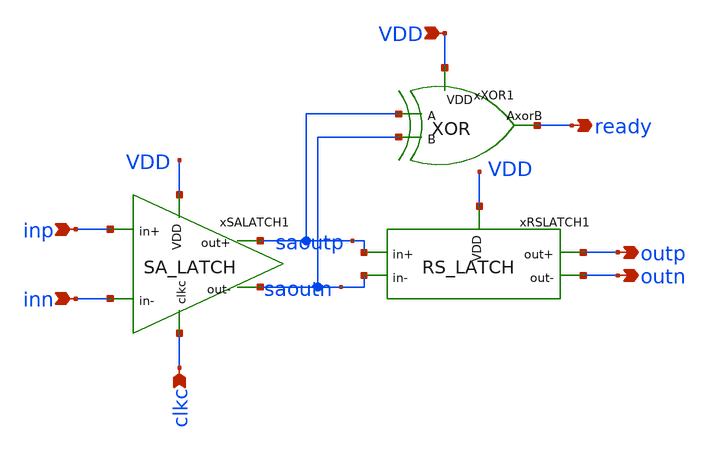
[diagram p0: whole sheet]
** sch_path: Design_Files/IC Design/Schematic/SAR_ADC_BLOCKS/COMP/COMP.sch
**.subckt COMP VDD inp inn outp outn clkc ready
*.ipin VDD
*.ipin inp
*.ipin inn
*.opin outp
*.opin outn
*.ipin clkc
*.opin ready
xXOR1 VDD ready saoutp saoutn XOR
xRSLATCH1 VDD outp outn saoutp saoutn RS_LATCH
xSALATCH1 VDD clkc saoutp saoutn inn inp SA_LATCH
**.ends

* expanding   symbol:  ECG_Acquisition_IC/Design_Files/IC
*+ Design/Schematic/SAR_ADC_BLOCKS/XOR/XOR.sym # of pins=4
** sym_path: Design_Files/IC Design/Schematic/SAR_ADC_BLOCKS/XOR/XOR.sym
** sch_path: Design_Files/IC Design/Schematic/SAR_ADC_BLOCKS/XOR/XOR.sch
.subckt XOR VDD AxorB A B
*.ipin VDD
*.ipin A
*.ipin B
*.opin AxorB
XM1 Abar A 0 0 nfet_03v3 L=0.28u W=0.5u nf=1 ad='int((nf+1)/2) * W/nf * 0.18u' as='int((nf+2)/2) * W/nf * 0.18u'
+ pd='2*int((nf+1)/2) * (W/nf + 0.18u)' ps='2*int((nf+2)/2) * (W/nf + 0.18u)' nrd='0.18u / W' nrs='0.18u / W'
+ sa=0 sb=0 sd=0 m=1
XM2 Abar A VDD VDD pfet_03v3 L=0.28u W=1u nf=1 ad='int((nf+1)/2) * W/nf * 0.18u' as='int((nf+2)/2) * W/nf * 0.18u'
+ pd='2*int((nf+1)/2) * (W/nf + 0.18u)' ps='2*int((nf+2)/2) * (W/nf + 0.18u)' nrd='0.18u / W' nrs='0.18u / W'
+ sa=0 sb=0 sd=0 m=1
XM3 Bbar B 0 0 nfet_03v3 L=0.28u W=0.5u nf=1 ad='int((nf+1)/2) * W/nf * 0.18u' as='int((nf+2)/2) * W/nf * 0.18u'
+ pd='2*int((nf+1)/2) * (W/nf + 0.18u)' ps='2*int((nf+2)/2) * (W/nf + 0.18u)' nrd='0.18u / W' nrs='0.18u / W'
+ sa=0 sb=0 sd=0 m=1
XM4 Bbar B VDD VDD pfet_03v3 L=0.28u W=1u nf=1 ad='int((nf+1)/2) * W/nf * 0.18u' as='int((nf+2)/2) * W/nf * 0.18u'
+ pd='2*int((nf+1)/2) * (W/nf + 0.18u)' ps='2*int((nf+2)/2) * (W/nf + 0.18u)' nrd='0.18u / W' nrs='0.18u / W'
+ sa=0 sb=0 sd=0 m=1
XM5 net1 Abar VDD VDD pfet_03v3 L=0.28u W=1.6u nf=1 ad='int((nf+1)/2) * W/nf * 0.18u' as='int((nf+2)/2) * W/nf * 0.18u'
+ pd='2*int((nf+1)/2) * (W/nf + 0.18u)' ps='2*int((nf+2)/2) * (W/nf + 0.18u)' nrd='0.18u / W' nrs='0.18u / W'
+ sa=0 sb=0 sd=0 m=1
XM6 AxorB B net1 VDD pfet_03v3 L=0.28u W=1.6u nf=1 ad='int((nf+1)/2) * W/nf * 0.18u' as='int((nf+2)/2) * W/nf * 0.18u'
+ pd='2*int((nf+1)/2) * (W/nf + 0.18u)' ps='2*int((nf+2)/2) * (W/nf + 0.18u)' nrd='0.18u / W' nrs='0.18u / W'
+ sa=0 sb=0 sd=0 m=1
XM7 net2 A VDD VDD pfet_03v3 L=0.28u W=1.6u nf=1 ad='int((nf+1)/2) * W/nf * 0.18u' as='int((nf+2)/2) * W/nf * 0.18u'
+ pd='2*int((nf+1)/2) * (W/nf + 0.18u)' ps='2*int((nf+2)/2) * (W/nf + 0.18u)' nrd='0.18u / W' nrs='0.18u / W'
+ sa=0 sb=0 sd=0 m=1
XM8 AxorB Bbar net2 VDD pfet_03v3 L=0.28u W=1.6u nf=1 ad='int((nf+1)/2) * W/nf * 0.18u' as='int((nf+2)/2) * W/nf * 0.18u'
+ pd='2*int((nf+1)/2) * (W/nf + 0.18u)' ps='2*int((nf+2)/2) * (W/nf + 0.18u)' nrd='0.18u / W' nrs='0.18u / W'
+ sa=0 sb=0 sd=0 m=1
XM9 AxorB A net3 0 nfet_03v3 L=0.28u W=0.8u nf=1 ad='int((nf+1)/2) * W/nf * 0.18u' as='int((nf+2)/2) * W/nf * 0.18u'
+ pd='2*int((nf+1)/2) * (W/nf + 0.18u)' ps='2*int((nf+2)/2) * (W/nf + 0.18u)' nrd='0.18u / W' nrs='0.18u / W'
+ sa=0 sb=0 sd=0 m=1
XM10 AxorB Abar net4 0 nfet_03v3 L=0.28u W=0.8u nf=1 ad='int((nf+1)/2) * W/nf * 0.18u' as='int((nf+2)/2) * W/nf * 0.18u'
+ pd='2*int((nf+1)/2) * (W/nf + 0.18u)' ps='2*int((nf+2)/2) * (W/nf + 0.18u)' nrd='0.18u / W' nrs='0.18u / W'
+ sa=0 sb=0 sd=0 m=1
XM11 net3 B 0 0 nfet_03v3 L=0.28u W=0.8u nf=1 ad='int((nf+1)/2) * W/nf * 0.18u' as='int((nf+2)/2) * W/nf * 0.18u'
+ pd='2*int((nf+1)/2) * (W/nf + 0.18u)' ps='2*int((nf+2)/2) * (W/nf + 0.18u)' nrd='0.18u / W' nrs='0.18u / W'
+ sa=0 sb=0 sd=0 m=1
XM12 net4 Bbar 0 0 nfet_03v3 L=0.28u W=0.8u nf=1 ad='int((nf+1)/2) * W/nf * 0.18u' as='int((nf+2)/2) * W/nf * 0.18u'
+ pd='2*int((nf+1)/2) * (W/nf + 0.18u)' ps='2*int((nf+2)/2) * (W/nf + 0.18u)' nrd='0.18u / W' nrs='0.18u / W'
+ sa=0 sb=0 sd=0 m=1
.ends


* expanding   symbol:  ECG_Acquisition_IC/Design_Files/IC
*+ Design/Schematic/SAR_ADC_BLOCKS/RS_LATCH/RS_LATCH.sym # of pins=5
** sym_path: Design_Files/IC Design/Schematic/SAR_ADC_BLOCKS/RS_LATCH/RS_LATCH.sym
** sch_path: Design_Files/IC Design/Schematic/SAR_ADC_BLOCKS/RS_LATCH/RS_LATCH.sch
.subckt RS_LATCH VDD out+ out- in+ in-
*.ipin VDD
*.ipin in+
*.ipin in-
*.opin out+
*.opin out-
XM4 out- out+ VDD VDD pfet_03v3 L=0.28u W=1u nf=1 ad='int((nf+1)/2) * W/nf * 0.18u' as='int((nf+2)/2) * W/nf * 0.18u'
+ pd='2*int((nf+1)/2) * (W/nf + 0.18u)' ps='2*int((nf+2)/2) * (W/nf + 0.18u)' nrd='0.18u / W' nrs='0.18u / W'
+ sa=0 sb=0 sd=0 m=1
XM8 out- out+ 0 0 nfet_03v3 L=0.28u W=0.3u nf=1 ad='int((nf+1)/2) * W/nf * 0.18u' as='int((nf+2)/2) * W/nf * 0.18u'
+ pd='2*int((nf+1)/2) * (W/nf + 0.18u)' ps='2*int((nf+2)/2) * (W/nf + 0.18u)' nrd='0.18u / W' nrs='0.18u / W'
+ sa=0 sb=0 sd=0 m=1
XM9 out+ net1 0 0 nfet_03v3 L=0.28u W=1u nf=1 ad='int((nf+1)/2) * W/nf * 0.18u' as='int((nf+2)/2) * W/nf * 0.18u'
+ pd='2*int((nf+1)/2) * (W/nf + 0.18u)' ps='2*int((nf+2)/2) * (W/nf + 0.18u)' nrd='0.18u / W' nrs='0.18u / W'
+ sa=0 sb=0 sd=0 m=1
XM5 out+ out- 0 0 nfet_03v3 L=0.28u W=0.3u nf=1 ad='int((nf+1)/2) * W/nf * 0.18u' as='int((nf+2)/2) * W/nf * 0.18u'
+ pd='2*int((nf+1)/2) * (W/nf + 0.18u)' ps='2*int((nf+2)/2) * (W/nf + 0.18u)' nrd='0.18u / W' nrs='0.18u / W'
+ sa=0 sb=0 sd=0 m=1
XM7 out- net2 0 0 nfet_03v3 L=0.28u W=1u nf=1 ad='int((nf+1)/2) * W/nf * 0.18u' as='int((nf+2)/2) * W/nf * 0.18u'
+ pd='2*int((nf+1)/2) * (W/nf + 0.18u)' ps='2*int((nf+2)/2) * (W/nf + 0.18u)' nrd='0.18u / W' nrs='0.18u / W'
+ sa=0 sb=0 sd=0 m=1
XM1 out+ out- VDD VDD pfet_03v3 L=0.28u W=1u nf=1 ad='int((nf+1)/2) * W/nf * 0.18u' as='int((nf+2)/2) * W/nf * 0.18u'
+ pd='2*int((nf+1)/2) * (W/nf + 0.18u)' ps='2*int((nf+2)/2) * (W/nf + 0.18u)' nrd='0.18u / W' nrs='0.18u / W'
+ sa=0 sb=0 sd=0 m=1
XM2 net1 in+ VDD VDD pfet_03v3 L=0.28u W=1u nf=1 ad='int((nf+1)/2) * W/nf * 0.18u' as='int((nf+2)/2) * W/nf * 0.18u'
+ pd='2*int((nf+1)/2) * (W/nf + 0.18u)' ps='2*int((nf+2)/2) * (W/nf + 0.18u)' nrd='0.18u / W' nrs='0.18u / W'
+ sa=0 sb=0 sd=0 m=1
XM3 net1 in+ 0 0 nfet_03v3 L=0.28u W=0.3u nf=1 ad='int((nf+1)/2) * W/nf * 0.18u' as='int((nf+2)/2) * W/nf * 0.18u'
+ pd='2*int((nf+1)/2) * (W/nf + 0.18u)' ps='2*int((nf+2)/2) * (W/nf + 0.18u)' nrd='0.18u / W' nrs='0.18u / W'
+ sa=0 sb=0 sd=0 m=1
XM6 net2 in- 0 0 nfet_03v3 L=0.28u W=0.3u nf=1 ad='int((nf+1)/2) * W/nf * 0.18u' as='int((nf+2)/2) * W/nf * 0.18u'
+ pd='2*int((nf+1)/2) * (W/nf + 0.18u)' ps='2*int((nf+2)/2) * (W/nf + 0.18u)' nrd='0.18u / W' nrs='0.18u / W'
+ sa=0 sb=0 sd=0 m=1
XM10 net2 in- VDD VDD pfet_03v3 L=0.28u W=1u nf=1 ad='int((nf+1)/2) * W/nf * 0.18u' as='int((nf+2)/2) * W/nf * 0.18u'
+ pd='2*int((nf+1)/2) * (W/nf + 0.18u)' ps='2*int((nf+2)/2) * (W/nf + 0.18u)' nrd='0.18u / W' nrs='0.18u / W'
+ sa=0 sb=0 sd=0 m=1
.ends


* expanding   symbol:  ECG_Acquisition_IC/Design_Files/IC
*+ Design/Schematic/SAR_ADC_BLOCKS/SA_LATCH/SA_LATCH.sym # of pins=6
** sym_path: Design_Files/IC Design/Schematic/SAR_ADC_BLOCKS/SA_LATCH/SA_LATCH.sym
** sch_path: Design_Files/IC Design/Schematic/SAR_ADC_BLOCKS/SA_LATCH/SA_LATCH.sch
.subckt SA_LATCH VDD clkc out+ out- in- in+
*.ipin VDD
*.opin out+
*.opin out-
*.ipin clkc
*.ipin in+
*.ipin in-
XM1 intp in+ net1 0 nfet_03v3 L=0.28u W=4u nf=1 ad='int((nf+1)/2) * W/nf * 0.18u' as='int((nf+2)/2) * W/nf * 0.18u'
+ pd='2*int((nf+1)/2) * (W/nf + 0.18u)' ps='2*int((nf+2)/2) * (W/nf + 0.18u)' nrd='0.18u / W' nrs='0.18u / W'
+ sa=0 sb=0 sd=0 m=1
XM3 out+ out- intn 0 nfet_03v3 L=0.28u W=1.2u nf=1 ad='int((nf+1)/2) * W/nf * 0.18u' as='int((nf+2)/2) * W/nf * 0.18u'
+ pd='2*int((nf+1)/2) * (W/nf + 0.18u)' ps='2*int((nf+2)/2) * (W/nf + 0.18u)' nrd='0.18u / W' nrs='0.18u / W'
+ sa=0 sb=0 sd=0 m=1
XM5 net1 clkc 0 0 nfet_03v3 L=0.28u W=1u nf=1 ad='int((nf+1)/2) * W/nf * 0.18u' as='int((nf+2)/2) * W/nf * 0.18u'
+ pd='2*int((nf+1)/2) * (W/nf + 0.18u)' ps='2*int((nf+2)/2) * (W/nf + 0.18u)' nrd='0.18u / W' nrs='0.18u / W'
+ sa=0 sb=0 sd=0 m=1
XM7 out+ out- VDD VDD pfet_03v3 L=0.28u W=1.5u nf=1 ad='int((nf+1)/2) * W/nf * 0.18u' as='int((nf+2)/2) * W/nf * 0.18u'
+ pd='2*int((nf+1)/2) * (W/nf + 0.18u)' ps='2*int((nf+2)/2) * (W/nf + 0.18u)' nrd='0.18u / W' nrs='0.18u / W'
+ sa=0 sb=0 sd=0 m=1
XM4 out- clkc VDD VDD pfet_03v3 L=0.28u W=0.8u nf=1 ad='int((nf+1)/2) * W/nf * 0.18u' as='int((nf+2)/2) * W/nf * 0.18u'
+ pd='2*int((nf+1)/2) * (W/nf + 0.18u)' ps='2*int((nf+2)/2) * (W/nf + 0.18u)' nrd='0.18u / W' nrs='0.18u / W'
+ sa=0 sb=0 sd=0 m=1
XM6 out- out+ VDD VDD pfet_03v3 L=0.28u W=1.5u nf=1 ad='int((nf+1)/2) * W/nf * 0.18u' as='int((nf+2)/2) * W/nf * 0.18u'
+ pd='2*int((nf+1)/2) * (W/nf + 0.18u)' ps='2*int((nf+2)/2) * (W/nf + 0.18u)' nrd='0.18u / W' nrs='0.18u / W'
+ sa=0 sb=0 sd=0 m=1
XM8 out+ clkc VDD VDD pfet_03v3 L=0.28u W=0.8u nf=1 ad='int((nf+1)/2) * W/nf * 0.18u' as='int((nf+2)/2) * W/nf * 0.18u'
+ pd='2*int((nf+1)/2) * (W/nf + 0.18u)' ps='2*int((nf+2)/2) * (W/nf + 0.18u)' nrd='0.18u / W' nrs='0.18u / W'
+ sa=0 sb=0 sd=0 m=1
XM9 out- out+ intp 0 nfet_03v3 L=0.28u W=1.2u nf=1 ad='int((nf+1)/2) * W/nf * 0.18u' as='int((nf+2)/2) * W/nf * 0.18u'
+ pd='2*int((nf+1)/2) * (W/nf + 0.18u)' ps='2*int((nf+2)/2) * (W/nf + 0.18u)' nrd='0.18u / W' nrs='0.18u / W'
+ sa=0 sb=0 sd=0 m=1
XM2 intn in- net1 0 nfet_03v3 L=0.28u W=4u nf=1 ad='int((nf+1)/2) * W/nf * 0.18u' as='int((nf+2)/2) * W/nf * 0.18u'
+ pd='2*int((nf+1)/2) * (W/nf + 0.18u)' ps='2*int((nf+2)/2) * (W/nf + 0.18u)' nrd='0.18u / W' nrs='0.18u / W'
+ sa=0 sb=0 sd=0 m=1
XM11 intn clkc intp VDD pfet_03v3 L=0.28u W=0.6u nf=1 ad='int((nf+1)/2) * W/nf * 0.18u' as='int((nf+2)/2) * W/nf * 0.18u'
+ pd='2*int((nf+1)/2) * (W/nf + 0.18u)' ps='2*int((nf+2)/2) * (W/nf + 0.18u)' nrd='0.18u / W' nrs='0.18u / W'
+ sa=0 sb=0 sd=0 m=1
.ends

.end
